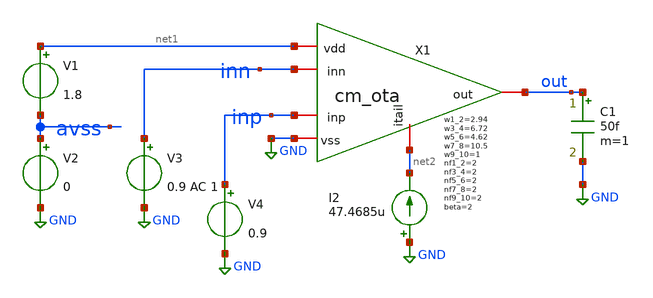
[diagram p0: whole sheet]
** sch_path: ISSCC25/submitted_notebooks/current_mirror_ota_optimization/characterization/sky130/schematics/tb_cm_ota_dcop.sch
**.subckt tb_cm_ota_dcop
V1 net1 avss 1.8
V2 avss GND 0
C1 out GND 50f m=1
V3 inn GND 0.9 AC 1
V4 inp GND 0.9
X1 net1 out inp inn net2 GND cm_ota w1_2=2.94 w3_4=6.72 w5_6=4.62 w7_8=10.5 w9_10=1 beta=2 nf1_2=2
+ nf3_4=2 nf5_6=2 nf7_8=2 nf9_10=2
I2 GND net2 47.4685u
**** begin user architecture code

** opencircuitdesign pdks isntsall
//.lib /opt/pdk/open_pdks/sky130/sky130A/libs.tech/ngspice/sky130.lib.spice tt




.lib /opt/pdk/open_pdks/sky130/sky130A/libs.tech/ngspice/sky130.lib.spice tt
.temp 27
.option savecurrents
.save all
.control
	op
	write tb_cm_ota_dcop.raw
	ac dec 100 10 10G
	run
	plot vdb(out) vs frequency
	plot 180*cph(out)/pi vs frequency
.endc


**** end user architecture code
**.ends

* expanding   symbol:  cm_ota.sym # of pins=6
** sym_path: ISSCC25/submitted_notebooks/current_mirror_ota_optimization/characterization/sky130/schematics/cm_ota.sym
** sch_path: ISSCC25/submitted_notebooks/current_mirror_ota_optimization/characterization/sky130/schematics/cm_ota.sch
.subckt cm_ota vdd out inp inn itail vss  w1_2=1 w3_4=1 w5_6=1 w7_8=1 w9_10=1 beta=2 nf1_2=2 nf3_4=2
+ nf5_6=2 nf7_8=2 nf9_10=2
*.iopin inn
*.iopin inp
*.iopin out
*.iopin vss
*.iopin vdd
*.iopin itail
XM1 ds1_3 inn source source sky130_fd_pr__nfet_01v8 L=0.15 W=w1_2 nf=nf1_2 ad='int((nf+1)/2) * W/nf * 0.29'
+ as='int((nf+2)/2) * W/nf * 0.29' pd='2*int((nf+1)/2) * (W/nf + 0.29)' ps='2*int((nf+2)/2) * (W/nf + 0.29)'
+ nrd='0.29 / W' nrs='0.29 / W' sa=0 sb=0 sd=0 mult=1 m=1
xM3 ds1_3 ds1_3 vdd vdd sky130_fd_pr__pfet_01v8 L=0.15 W=w3_4 nf=nf3_4 ad='int((nf+1)/2) * W/nf * 0.29'
+ as='int((nf+2)/2) * W/nf * 0.29' pd='2*int((nf+1)/2) * (W/nf + 0.29)' ps='2*int((nf+2)/2) * (W/nf + 0.29)'
+ nrd='0.29 / W' nrs='0.29 / W' sa=0 sb=0 sd=0 mult=1 m=1
XM2 ds2_4 inp source source sky130_fd_pr__nfet_01v8 L=0.15 W=w1_2 nf=nf1_2 ad='int((nf+1)/2) * W/nf * 0.29'
+ as='int((nf+2)/2) * W/nf * 0.29' pd='2*int((nf+1)/2) * (W/nf + 0.29)' ps='2*int((nf+2)/2) * (W/nf + 0.29)'
+ nrd='0.29 / W' nrs='0.29 / W' sa=0 sb=0 sd=0 mult=1 m=1
xM4 ds2_4 ds2_4 vdd vdd sky130_fd_pr__pfet_01v8 L=0.15 W=w3_4 nf=nf3_4 ad='int((nf+1)/2) * W/nf * 0.29'
+ as='int((nf+2)/2) * W/nf * 0.29' pd='2*int((nf+1)/2) * (W/nf + 0.29)' ps='2*int((nf+2)/2) * (W/nf + 0.29)'
+ nrd='0.29 / W' nrs='0.29 / W' sa=0 sb=0 sd=0 mult=1 m=1
xM7 ds5_7 ds1_3 vdd vdd sky130_fd_pr__pfet_01v8 L=0.15 W=w7_8 nf=nf7_8 ad='int((nf+1)/2) * W/nf * 0.29'
+ as='int((nf+2)/2) * W/nf * 0.29' pd='2*int((nf+1)/2) * (W/nf + 0.29)' ps='2*int((nf+2)/2) * (W/nf + 0.29)'
+ nrd='0.29 / W' nrs='0.29 / W' sa=0 sb=0 sd=0 mult=1 m=1
XM5 ds5_7 ds5_7 vss vss sky130_fd_pr__nfet_01v8 L=0.15 W=w5_6 nf=nf5_6 ad='int((nf+1)/2) * W/nf * 0.29'
+ as='int((nf+2)/2) * W/nf * 0.29' pd='2*int((nf+1)/2) * (W/nf + 0.29)' ps='2*int((nf+2)/2) * (W/nf + 0.29)'
+ nrd='0.29 / W' nrs='0.29 / W' sa=0 sb=0 sd=0 mult=1 m=1
XM6 out ds5_7 vss vss sky130_fd_pr__nfet_01v8 L=0.15 W=w5_6 nf=nf5_6 ad='int((nf+1)/2) * W/nf * 0.29'
+ as='int((nf+2)/2) * W/nf * 0.29' pd='2*int((nf+1)/2) * (W/nf + 0.29)' ps='2*int((nf+2)/2) * (W/nf + 0.29)'
+ nrd='0.29 / W' nrs='0.29 / W' sa=0 sb=0 sd=0 mult=1 m=1
xM8 out ds2_4 vdd vdd sky130_fd_pr__pfet_01v8 L=0.15 W=w7_8 nf=nf7_8 ad='int((nf+1)/2) * W/nf * 0.29'
+ as='int((nf+2)/2) * W/nf * 0.29' pd='2*int((nf+1)/2) * (W/nf + 0.29)' ps='2*int((nf+2)/2) * (W/nf + 0.29)'
+ nrd='0.29 / W' nrs='0.29 / W' sa=0 sb=0 sd=0 mult=1 m=1
XM9 source itail vss vss sky130_fd_pr__nfet_01v8 L=0.15 W=w9_10 nf=nf9_10 ad='int((nf+1)/2) * W/nf * 0.29'
+ as='int((nf+2)/2) * W/nf * 0.29' pd='2*int((nf+1)/2) * (W/nf + 0.29)' ps='2*int((nf+2)/2) * (W/nf + 0.29)'
+ nrd='0.29 / W' nrs='0.29 / W' sa=0 sb=0 sd=0 mult=1 m=1
XM10 itail itail vss vss sky130_fd_pr__nfet_01v8 L=0.15 W=w9_10 nf=nf1_2 ad='int((nf+1)/2) * W/nf * 0.29'
+ as='int((nf+2)/2) * W/nf * 0.29' pd='2*int((nf+1)/2) * (W/nf + 0.29)' ps='2*int((nf+2)/2) * (W/nf + 0.29)'
+ nrd='0.29 / W' nrs='0.29 / W' sa=0 sb=0 sd=0 mult=1 m=1
.ends

.GLOBAL GND
.end
